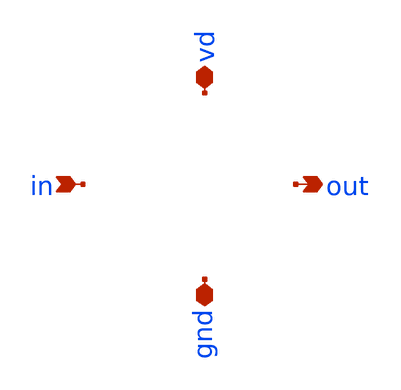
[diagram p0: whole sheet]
** sch_path: xschem/inverter-sky130-pex.sch
**.subckt inverter-sky130-pex in vd gnd out
*.ipin in
*.iopin vd
*.iopin gnd
*.opin out
**** begin user architecture code


* NGSPICE file created from inverter-sky130.ext - technology: sky130A

*.subckt inverter-sky130 in vd gnd out
X0 out.t0 in.t0 vd.t1 vd.t0 sky130_fd_pr__pfet_01v8 ad=0.87 pd=6.58 as=0.87 ps=6.58 w=3 l=0.15
X1 out.t1 in.t1 gnd.t1 gnd.t0 sky130_fd_pr__nfet_01v8 ad=0.29 pd=2.58 as=0.29 ps=2.58 w=1 l=0.15
R0 in.n0 in.t0 569.664
R1 in.n0 in.t1 233.871
R2 in in.n0 0.813
R3 vd.n2 vd.n1 135.465
R4 vd.n9 vd.n8 113.319
R5 vd.n5 vd.n4 113.319
R6 vd.n16 vd.t1 9.59734
R7 vd vd.n16 0.246125
R8 vd.n13 vd.n6 0.0678069
R9 vd.n11 vd.n10 0.0678063
R10 vd.n10 vd.n9 0.0673111
R11 vd.n6 vd.n5 0.0673111
R12 vd.n8 vd.n7 0.0349892
R13 vd.n7 vd.t0 0.0349892
R14 vd.n4 vd.n3 0.0349892
R15 vd.n3 vd.n2 0.0333079
R16 vd.n1 vd.n0 0.00627981
R17 vd.n16 vd.n15 0.00376374
R18 vd.n14 vd.n13 0.00203361
R19 vd.n15 vd.n14 0.00144883
R20 vd.n12 vd.n11 0.00100072
R21 vd.n13 vd.n12 0.00100006
R22 out out.t1 17.7269
R23 out out.t0 10.2205
R24 gnd.n8 gnd.n6 149.835
R25 gnd.n9 gnd.n8 93.7417
R26 gnd.n3 gnd.n2 93.7417
R27 gnd.n16 gnd.t1 17.4924
R28 gnd.n10 gnd.n9 1.1255
R29 gnd.n4 gnd.n3 1.1255
R30 gnd.n13 gnd.n4 1.12453
R31 gnd.n11 gnd.n10 1.12443
R32 gnd gnd.n16 0.233625
R33 gnd.n8 gnd.n7 0.10956
R34 gnd.n7 gnd.t0 0.10956
R35 gnd.n2 gnd.n1 0.10956
R36 gnd.n1 gnd.n0 0.077227
R37 gnd.n6 gnd.n5 0.0425017
R38 gnd.n14 gnd.n13 0.00308435
R39 gnd.n15 gnd.n14 0.00253648
R40 gnd.n16 gnd.n15 0.0016032
R41 gnd.n12 gnd.n11 0.00110931
R42 gnd.n13 gnd.n12 0.00100272
C0 in out 0.141f
C1 out vd 0.769f
C2 in vd 0.411f
*.ends



**** end user architecture code
**.ends
.end
